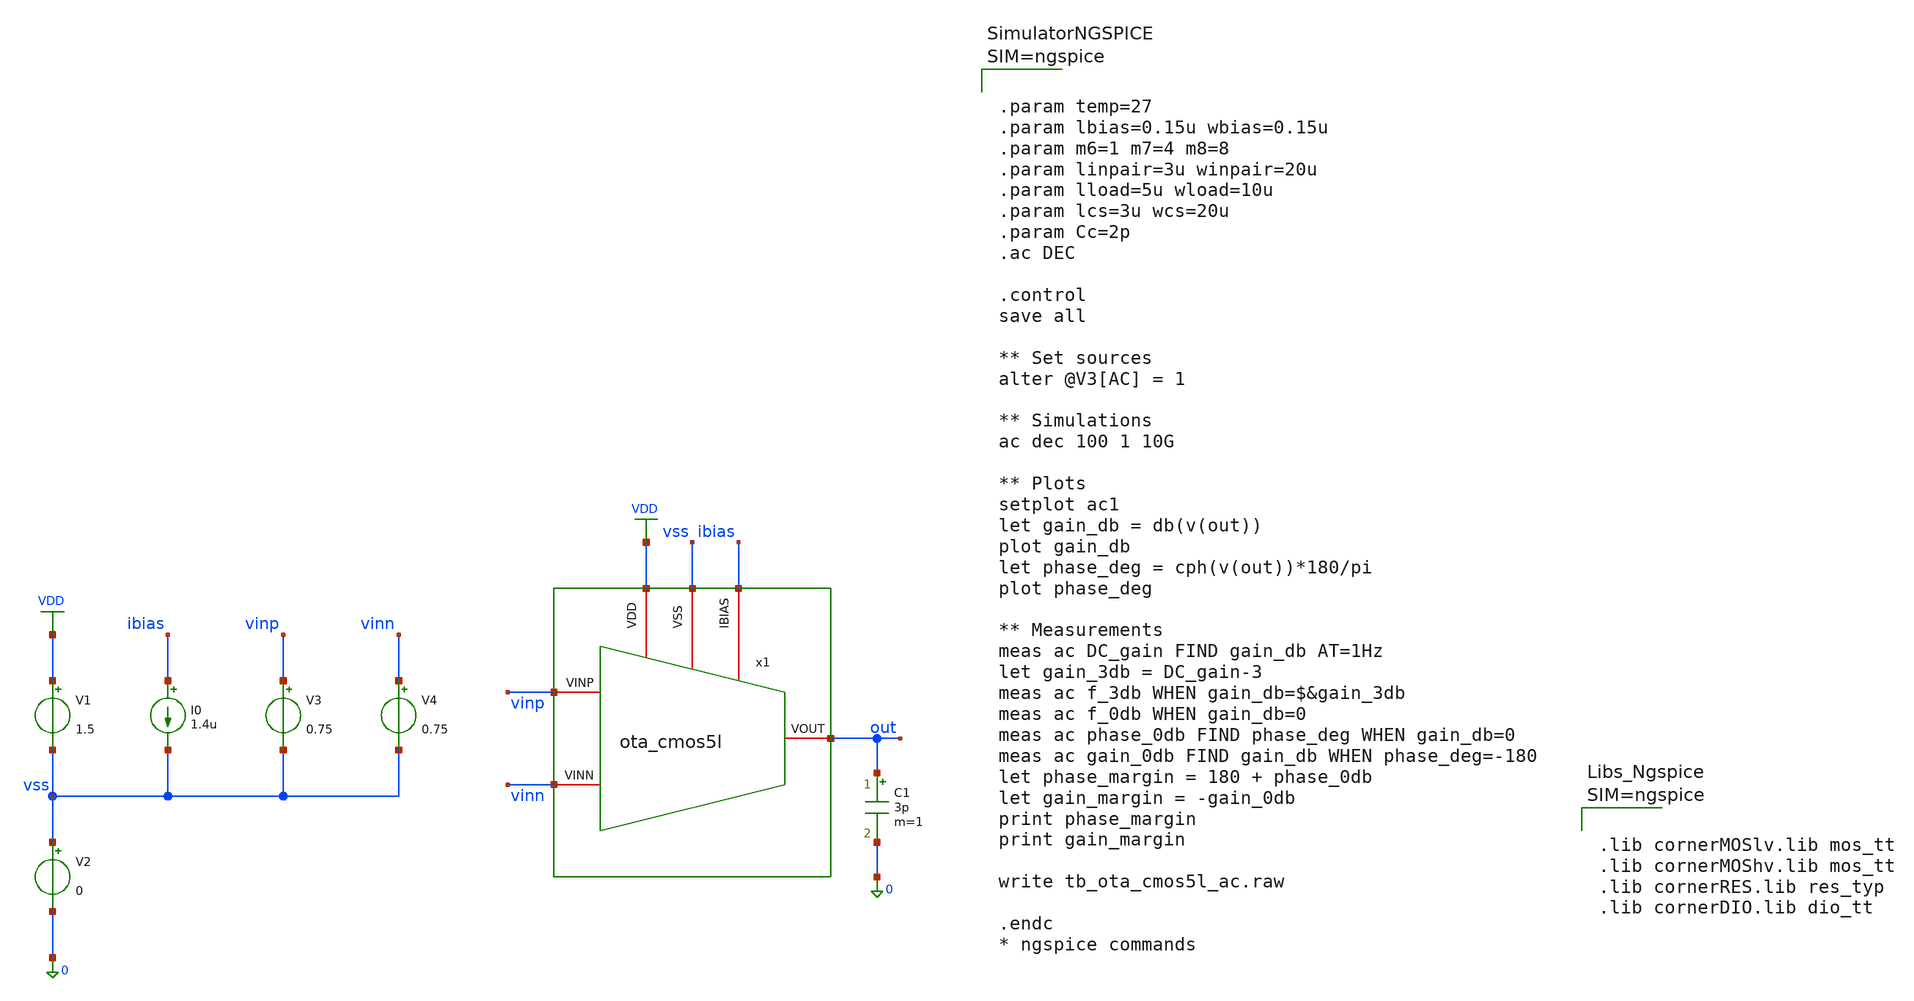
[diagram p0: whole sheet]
** sch_path: xschem/ota_cmos5l/tb/tb_ota_cmos5l_ac/tb_ota_cmos5l_ac.sch
**.subckt tb_ota_cmos5l_ac
x1 vss ibias VDD vinn vinp out ota_cmos5l
C1 out 0 3p m=1
I0 ibias vss 1.4u
V1 VDD vss 1.5
V2 vss 0 0
V3 vinp vss 0.75
V4 vinn vss 0.75
**** begin user architecture code



.param temp=27
.param lbias=0.15u wbias=0.15u
.param m6=1 m7=4 m8=8
.param linpair=3u winpair=20u
.param lload=5u wload=10u
.param lcs=3u wcs=20u
.param Cc=2p
.ac DEC

.control
save all

** Set sources
alter @V3[AC] = 1

** Simulations
ac dec 100 1 10G

** Plots
setplot ac1
let gain_db = db(v(out))
plot gain_db
let phase_deg = cph(v(out))*180/pi
plot phase_deg

** Measurements
meas ac DC_gain FIND gain_db AT=1Hz
let gain_3db = DC_gain-3
meas ac f_3db WHEN gain_db=$&gain_3db
meas ac f_0db WHEN gain_db=0
meas ac phase_0db FIND phase_deg WHEN gain_db=0
meas ac gain_0db FIND gain_db WHEN phase_deg=-180
let phase_margin = 180 + phase_0db
let gain_margin = -gain_0db
print phase_margin
print gain_margin

write tb_ota_cmos5l_ac.raw

.endc
* ngspice commands






.lib cornerMOSlv.lib mos_tt
.lib cornerMOShv.lib mos_tt
.lib cornerRES.lib res_typ
.lib cornerDIO.lib dio_tt



**** end user architecture code
**.ends

* expanding   symbol:  /foss/designs/sg13cmos5l_spma_ip__instramp/xschem/ota_cmos5l/ota_cmos5l.sym #
*+ of pins=6
** sym_path: xschem/output_buffer/ota_cmos5l.sym
** sch_path: xschem/output_buffer/ota_cmos5l.sch
.subckt ota_cmos5l VSS IBIAS VDD VINN VINP VOUT
*.iopin IBIAS
*.iopin VDD
*.iopin VSS
*.iopin VOUT
*.iopin VINP
*.iopin VINN
XM6 IBIAS IBIAS VDD VDD sg13_lv_pmos w={wbias} l={lbias} ng=1 m={m6} mm_ok=1
XM7 net1 IBIAS VDD VDD sg13_lv_pmos w={wbias} l={lbias} ng=1 m={m7} mm_ok=1
XM8 VOUT IBIAS VDD VDD sg13_lv_pmos w={wbias} l={lbias} ng=1 m={m8} mm_ok=1
XM1 net2 VINN net1 VDD sg13_lv_pmos w={winpair} l={linpair} ng=1 m=1 mm_ok=1
XM2 net3 VINP net1 VDD sg13_lv_pmos w={winpair} l={linpair} ng=1 m=1 mm_ok=1
XM3 net2 net2 VSS VSS sg13_lv_nmos w={wload} l={lload} ng=1 m=1 mm_ok=1
XM4 net3 net2 VSS VSS sg13_lv_nmos w={wload} l={lload} ng=1 m=1 mm_ok=1
XM5 VOUT net3 VSS VSS sg13_lv_nmos w={wcs} l={lcs} ng=1 m=1 mm_ok=1
XR1 net3 net4 VSS rhigh w=0.5e-6 l=1.95e-6 m=1 b=0 mm_ok=1
.save v(vinp)
.save v(vinn)
.save v(vout)
XC2 VOUT net4 cap_cmomi w=15e-6 l=15e-6 mmin=1 mmax=4 feed=double subblock=0 m=5 mm_ok=1
**** begin user architecture code


.param temp=27
.param lbias=0.15u wbias=0.15u
.param m6=1 m7=4 m8=8
.param linpair=3u winpair=20u
.param lload=5u wload=10u
.param lcs=3u wcs=20u
.param Cc=2p



**** end user architecture code
XC1 VOUT net4 cap_cmomi w=15e-6 l=15e-6 mmin=1 mmax=4 feed=double subblock=0 m=4 mm_ok=1
.ends

.GLOBAL VDD
.end
